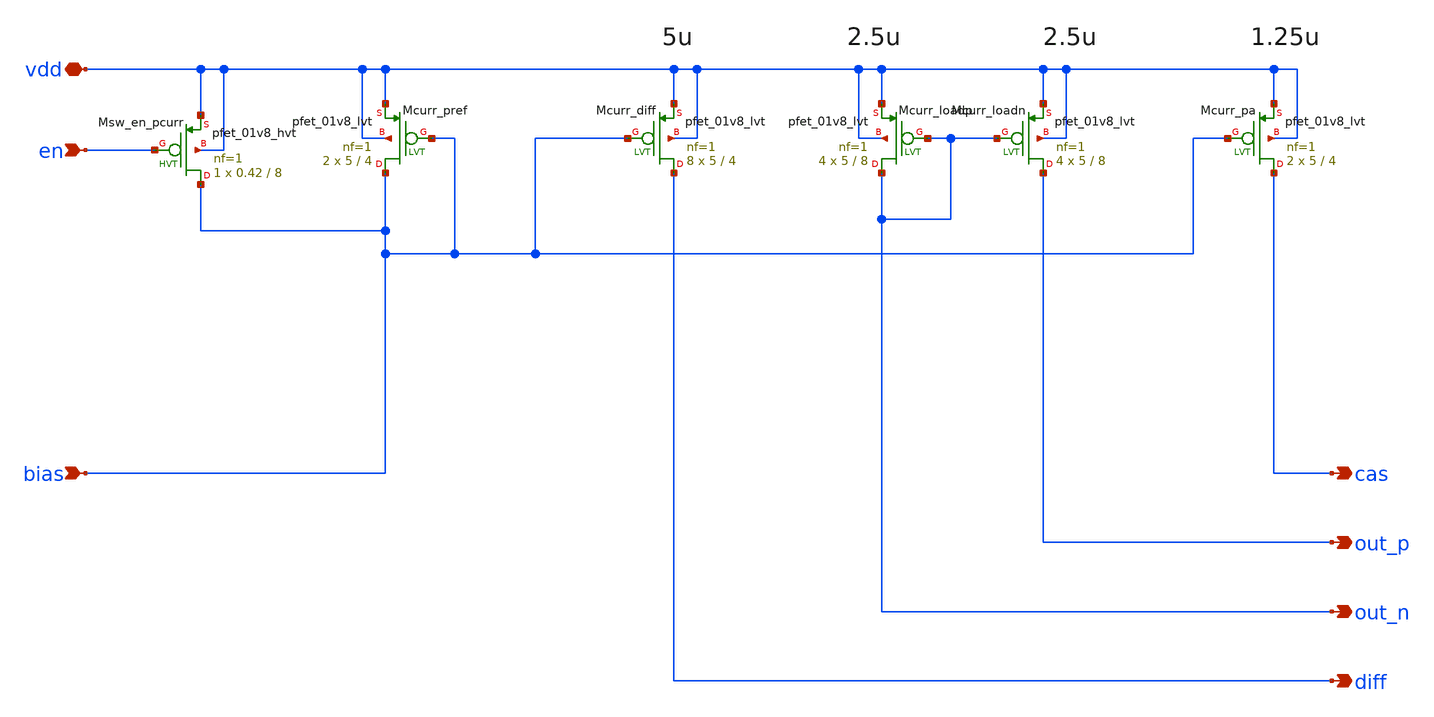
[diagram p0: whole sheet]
** sch_path: design/bandgap_opamp_pmos/bandgap_opamp_pmos.sch
**.subckt bandgap_opamp_pmos bias out_p vdd en out_n cas diff
*.ipin bias
*.opin out_p
*.iopin vdd
*.ipin en
*.opin out_n
*.opin cas
*.opin diff
XMcurr_diff diff bias vdd vdd sky130_fd_pr__pfet_01v8_lvt L=4 W=5 nf=1 ad='W * 0.29' as='W * 0.29' pd='2 * (W + 0.29)'
+ ps='2 * (W + 0.29)' nrd='0.29 / W' nrs='0.29 / W' sa=0 sb=0 sd=0 mult=8 m=8
XMcurr_pref bias bias vdd vdd sky130_fd_pr__pfet_01v8_lvt L=4 W=5 nf=1 ad='W * 0.29' as='W * 0.29' pd='2 * (W + 0.29)'
+ ps='2 * (W + 0.29)' nrd='0.29 / W' nrs='0.29 / W' sa=0 sb=0 sd=0 mult=2 m=2
XMcurr_pa cas bias vdd vdd sky130_fd_pr__pfet_01v8_lvt L=4 W=5 nf=1 ad='W * 0.29' as='W * 0.29' pd='2 * (W + 0.29)'
+ ps='2 * (W + 0.29)' nrd='0.29 / W' nrs='0.29 / W' sa=0 sb=0 sd=0 mult=2 m=2
XMcurr_loadp out_n out_n vdd vdd sky130_fd_pr__pfet_01v8_lvt L=8 W=5 nf=1 ad='W * 0.29' as='W * 0.29'
+ pd='2 * (W + 0.29)' ps='2 * (W + 0.29)' nrd='0.29 / W' nrs='0.29 / W' sa=0 sb=0 sd=0 mult=4 m=4
XMcurr_loadn out_p out_n vdd vdd sky130_fd_pr__pfet_01v8_lvt L=8 W=5 nf=1 ad='W * 0.29' as='W * 0.29'
+ pd='2 * (W + 0.29)' ps='2 * (W + 0.29)' nrd='0.29 / W' nrs='0.29 / W' sa=0 sb=0 sd=0 mult=4 m=4
XMsw_en_pcurr bias en vdd vdd sky130_fd_pr__pfet_01v8_hvt L=8 W=0.42 nf=1 ad='W * 0.29' as='W * 0.29'
+ pd='2 * (W + 0.29)' ps='2 * (W + 0.29)' nrd='0.29 / W' nrs='0.29 / W' sa=0 sb=0 sd=0 mult=1 m=1
**.ends
.end
